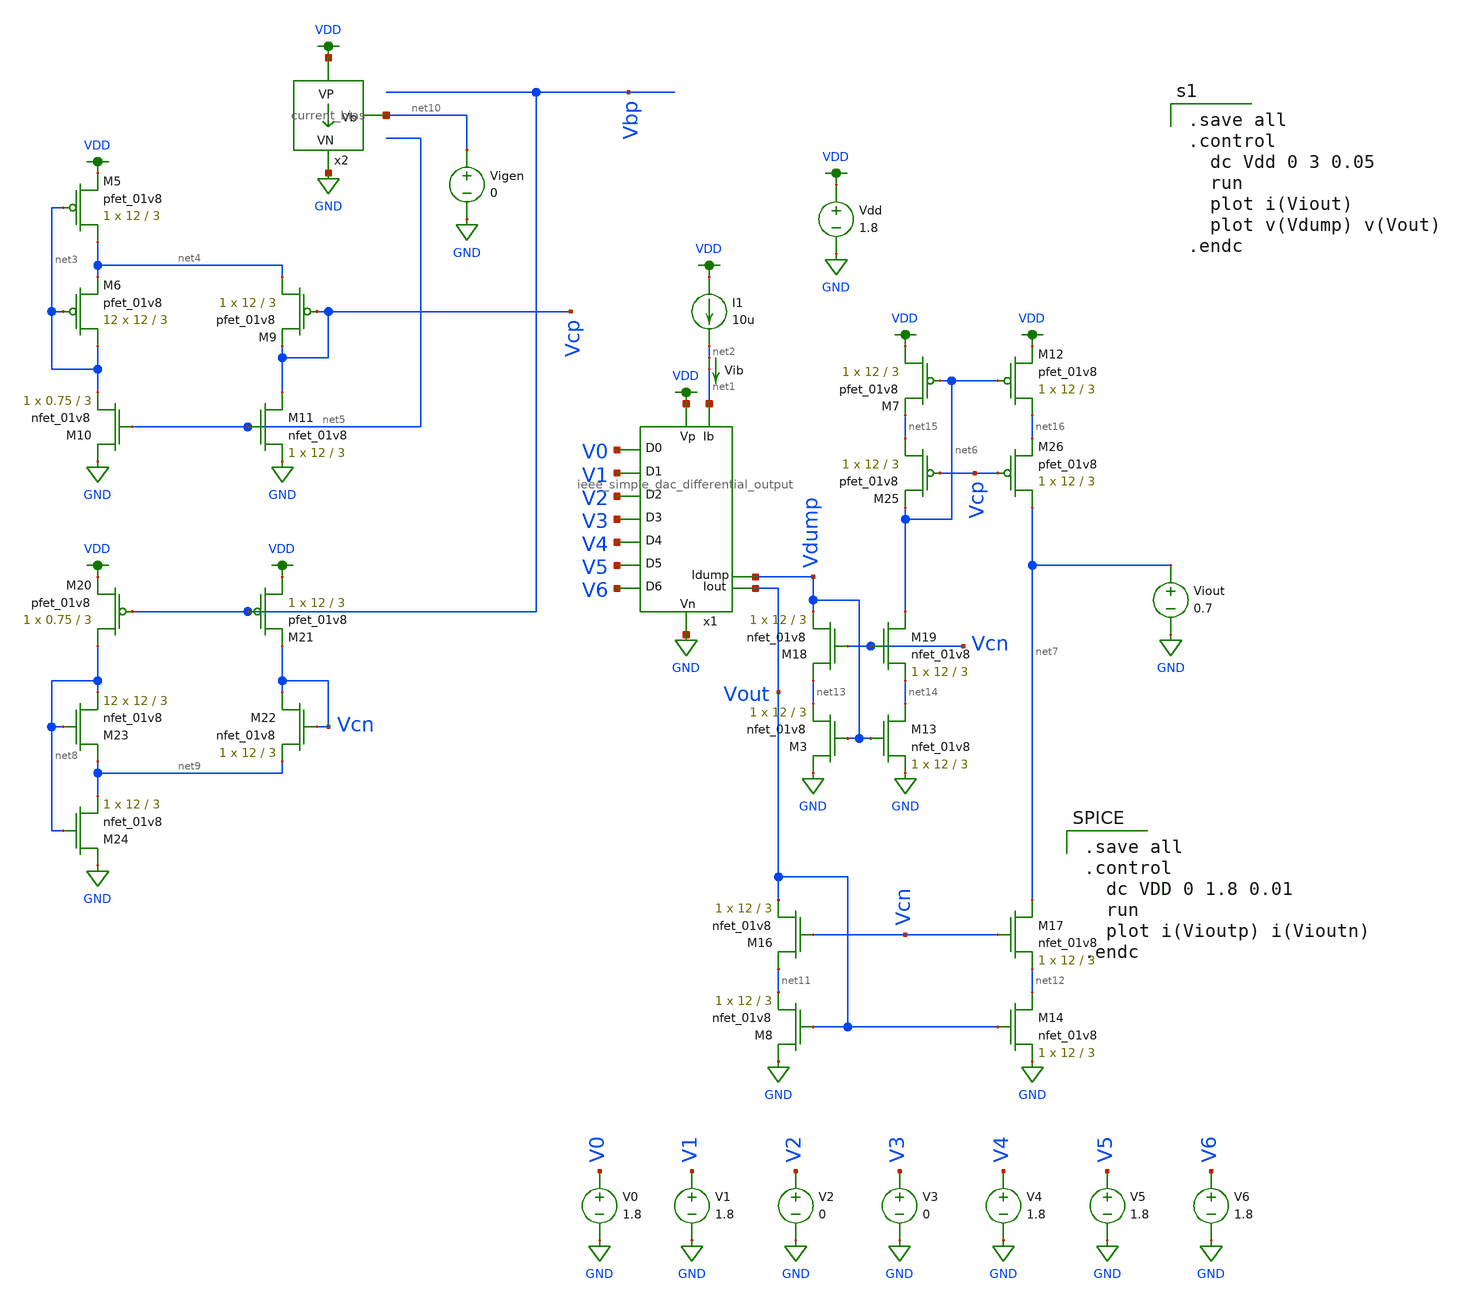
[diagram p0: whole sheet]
** sch_path: schematics/ieee DAC/ieee_DAC_mc_simulation_4.sch
**.subckt ieee_DAC_mc_simulation_4
Vdd VDD GND 1.8
V1 V1 GND 1.8
V2 V2 GND 0
V3 V3 GND 0
V4 V4 GND 1.8
V5 V5 GND 1.8
V6 V6 GND 1.8
V0 V0 GND 1.8
Vib net2 net1 0
.save i(vib)
XM5 net4 net3 VDD VDD sky130_fd_pr__pfet_01v8 L=3 W=12 nf=1 ad='int((nf+1)/2) * W/nf * 0.29' as='int((nf+2)/2) * W/nf * 0.29'
+ pd='2*int((nf+1)/2) * (W/nf + 0.29)' ps='2*int((nf+2)/2) * (W/nf + 0.29)' nrd='0.29 / W' nrs='0.29 / W'
+ sa=0 sb=0 sd=0 mult=1 m=1
XM6 net3 net3 net4 VDD sky130_fd_pr__pfet_01v8 L=3 W=12 nf=1 ad='int((nf+1)/2) * W/nf * 0.29' as='int((nf+2)/2) * W/nf * 0.29'
+ pd='2*int((nf+1)/2) * (W/nf + 0.29)' ps='2*int((nf+2)/2) * (W/nf + 0.29)' nrd='0.29 / W' nrs='0.29 / W'
+ sa=0 sb=0 sd=0 mult=12 m=12
XM9 net4 Vcp Vcp VDD sky130_fd_pr__pfet_01v8 L=3 W=12 nf=1 ad='int((nf+1)/2) * W/nf * 0.29' as='int((nf+2)/2) * W/nf * 0.29'
+ pd='2*int((nf+1)/2) * (W/nf + 0.29)' ps='2*int((nf+2)/2) * (W/nf + 0.29)' nrd='0.29 / W' nrs='0.29 / W'
+ sa=0 sb=0 sd=0 mult=1 m=1
XM10 GND net5 net3 GND sky130_fd_pr__nfet_01v8 L=3 W=0.75 nf=1 ad='int((nf+1)/2) * W/nf * 0.29' as='int((nf+2)/2) * W/nf * 0.29'
+ pd='2*int((nf+1)/2) * (W/nf + 0.29)' ps='2*int((nf+2)/2) * (W/nf + 0.29)' nrd='0.29 / W' nrs='0.29 / W'
+ sa=0 sb=0 sd=0 mult=1 m=1
XM11 Vcp net5 GND GND sky130_fd_pr__nfet_01v8 L=3 W=12 nf=1 ad='int((nf+1)/2) * W/nf * 0.29' as='int((nf+2)/2) * W/nf * 0.29'
+ pd='2*int((nf+1)/2) * (W/nf + 0.29)' ps='2*int((nf+2)/2) * (W/nf + 0.29)' nrd='0.29 / W' nrs='0.29 / W'
+ sa=0 sb=0 sd=0 mult=1 m=1
x2 VDD net10 GND current_bias
Vigen net10 GND 0
x1 VDD Vdump GND V1 V0 V2 V3 V4 V5 V6 net1 Vout ieee_simple_dac_differential_output
XM3 GND Vdump net13 GND sky130_fd_pr__nfet_01v8 L=3 W=12 nf=1 ad='int((nf+1)/2) * W/nf * 0.29' as='int((nf+2)/2) * W/nf * 0.29'
+ pd='2*int((nf+1)/2) * (W/nf + 0.29)' ps='2*int((nf+2)/2) * (W/nf + 0.29)' nrd='0.29 / W' nrs='0.29 / W'
+ sa=0 sb=0 sd=0 mult=1 m=1
XM7 VDD net6 net15 VDD sky130_fd_pr__pfet_01v8 L=3 W=12 nf=1 ad='int((nf+1)/2) * W/nf * 0.29' as='int((nf+2)/2) * W/nf * 0.29'
+ pd='2*int((nf+1)/2) * (W/nf + 0.29)' ps='2*int((nf+2)/2) * (W/nf + 0.29)' nrd='0.29 / W' nrs='0.29 / W'
+ sa=0 sb=0 sd=0 mult=1 m=1
XM8 GND Vout net11 GND sky130_fd_pr__nfet_01v8 L=3 W=12 nf=1 ad='int((nf+1)/2) * W/nf * 0.29' as='int((nf+2)/2) * W/nf * 0.29'
+ pd='2*int((nf+1)/2) * (W/nf + 0.29)' ps='2*int((nf+2)/2) * (W/nf + 0.29)' nrd='0.29 / W' nrs='0.29 / W'
+ sa=0 sb=0 sd=0 mult=1 m=1
XM12 net16 net6 VDD VDD sky130_fd_pr__pfet_01v8 L=3 W=12 nf=1 ad='int((nf+1)/2) * W/nf * 0.29' as='int((nf+2)/2) * W/nf * 0.29'
+ pd='2*int((nf+1)/2) * (W/nf + 0.29)' ps='2*int((nf+2)/2) * (W/nf + 0.29)' nrd='0.29 / W' nrs='0.29 / W'
+ sa=0 sb=0 sd=0 mult=1 m=1
Viout net7 GND 0.7
XM13 net14 Vdump GND GND sky130_fd_pr__nfet_01v8 L=3 W=12 nf=1 ad='int((nf+1)/2) * W/nf * 0.29' as='int((nf+2)/2) * W/nf * 0.29'
+ pd='2*int((nf+1)/2) * (W/nf + 0.29)' ps='2*int((nf+2)/2) * (W/nf + 0.29)' nrd='0.29 / W' nrs='0.29 / W'
+ sa=0 sb=0 sd=0 mult=1 m=1
XM14 net12 Vout GND GND sky130_fd_pr__nfet_01v8 L=3 W=12 nf=1 ad='int((nf+1)/2) * W/nf * 0.29' as='int((nf+2)/2) * W/nf * 0.29'
+ pd='2*int((nf+1)/2) * (W/nf + 0.29)' ps='2*int((nf+2)/2) * (W/nf + 0.29)' nrd='0.29 / W' nrs='0.29 / W'
+ sa=0 sb=0 sd=0 mult=1 m=1
XM20 net8 Vbp VDD VDD sky130_fd_pr__pfet_01v8 L=3 W=0.75 nf=1 ad='int((nf+1)/2) * W/nf * 0.29' as='int((nf+2)/2) * W/nf * 0.29'
+ pd='2*int((nf+1)/2) * (W/nf + 0.29)' ps='2*int((nf+2)/2) * (W/nf + 0.29)' nrd='0.29 / W' nrs='0.29 / W'
+ sa=0 sb=0 sd=0 mult=1 m=1
XM21 VDD Vbp Vcn VDD sky130_fd_pr__pfet_01v8 L=3 W=12 nf=1 ad='int((nf+1)/2) * W/nf * 0.29' as='int((nf+2)/2) * W/nf * 0.29'
+ pd='2*int((nf+1)/2) * (W/nf + 0.29)' ps='2*int((nf+2)/2) * (W/nf + 0.29)' nrd='0.29 / W' nrs='0.29 / W'
+ sa=0 sb=0 sd=0 mult=1 m=1
XM22 Vcn Vcn net9 GND sky130_fd_pr__nfet_01v8 L=3 W=12 nf=1 ad='int((nf+1)/2) * W/nf * 0.29' as='int((nf+2)/2) * W/nf * 0.29'
+ pd='2*int((nf+1)/2) * (W/nf + 0.29)' ps='2*int((nf+2)/2) * (W/nf + 0.29)' nrd='0.29 / W' nrs='0.29 / W'
+ sa=0 sb=0 sd=0 mult=1 m=1
XM23 net9 net8 net8 GND sky130_fd_pr__nfet_01v8 L=3 W=12 nf=1 ad='int((nf+1)/2) * W/nf * 0.29' as='int((nf+2)/2) * W/nf * 0.29'
+ pd='2*int((nf+1)/2) * (W/nf + 0.29)' ps='2*int((nf+2)/2) * (W/nf + 0.29)' nrd='0.29 / W' nrs='0.29 / W'
+ sa=0 sb=0 sd=0 mult=12 m=12
XM24 GND net8 net9 GND sky130_fd_pr__nfet_01v8 L=3 W=12 nf=1 ad='int((nf+1)/2) * W/nf * 0.29' as='int((nf+2)/2) * W/nf * 0.29'
+ pd='2*int((nf+1)/2) * (W/nf + 0.29)' ps='2*int((nf+2)/2) * (W/nf + 0.29)' nrd='0.29 / W' nrs='0.29 / W'
+ sa=0 sb=0 sd=0 mult=1 m=1
XM16 net11 Vcn Vout GND sky130_fd_pr__nfet_01v8 L=3 W=12 nf=1 ad='int((nf+1)/2) * W/nf * 0.29' as='int((nf+2)/2) * W/nf * 0.29'
+ pd='2*int((nf+1)/2) * (W/nf + 0.29)' ps='2*int((nf+2)/2) * (W/nf + 0.29)' nrd='0.29 / W' nrs='0.29 / W'
+ sa=0 sb=0 sd=0 mult=1 m=1
XM17 net7 Vcn net12 GND sky130_fd_pr__nfet_01v8 L=3 W=12 nf=1 ad='int((nf+1)/2) * W/nf * 0.29' as='int((nf+2)/2) * W/nf * 0.29'
+ pd='2*int((nf+1)/2) * (W/nf + 0.29)' ps='2*int((nf+2)/2) * (W/nf + 0.29)' nrd='0.29 / W' nrs='0.29 / W'
+ sa=0 sb=0 sd=0 mult=1 m=1
XM18 net13 Vcn Vdump GND sky130_fd_pr__nfet_01v8 L=3 W=12 nf=1 ad='int((nf+1)/2) * W/nf * 0.29' as='int((nf+2)/2) * W/nf * 0.29'
+ pd='2*int((nf+1)/2) * (W/nf + 0.29)' ps='2*int((nf+2)/2) * (W/nf + 0.29)' nrd='0.29 / W' nrs='0.29 / W'
+ sa=0 sb=0 sd=0 mult=1 m=1
XM19 net6 Vcn net14 GND sky130_fd_pr__nfet_01v8 L=3 W=12 nf=1 ad='int((nf+1)/2) * W/nf * 0.29' as='int((nf+2)/2) * W/nf * 0.29'
+ pd='2*int((nf+1)/2) * (W/nf + 0.29)' ps='2*int((nf+2)/2) * (W/nf + 0.29)' nrd='0.29 / W' nrs='0.29 / W'
+ sa=0 sb=0 sd=0 mult=1 m=1
XM25 net15 Vcp net6 VDD sky130_fd_pr__pfet_01v8 L=3 W=12 nf=1 ad='int((nf+1)/2) * W/nf * 0.29' as='int((nf+2)/2) * W/nf * 0.29'
+ pd='2*int((nf+1)/2) * (W/nf + 0.29)' ps='2*int((nf+2)/2) * (W/nf + 0.29)' nrd='0.29 / W' nrs='0.29 / W'
+ sa=0 sb=0 sd=0 mult=1 m=1
XM26 net7 Vcp net16 VDD sky130_fd_pr__pfet_01v8 L=3 W=12 nf=1 ad='int((nf+1)/2) * W/nf * 0.29' as='int((nf+2)/2) * W/nf * 0.29'
+ pd='2*int((nf+1)/2) * (W/nf + 0.29)' ps='2*int((nf+2)/2) * (W/nf + 0.29)' nrd='0.29 / W' nrs='0.29 / W'
+ sa=0 sb=0 sd=0 mult=1 m=1
I1 VDD net2 10u
**** begin user architecture code

.option wnflag=1
.param MC_SWITCH=1.0
.lib ~/skywater/skywater-pdk/libraries/sky130_fd_pr_ngspice/latest/models/sky130.lib.spice tt


.save all
.control
  dc Vdd 0 3 0.05
  run
  plot i(Viout)
  plot v(Vdump) v(Vout)
.endc


.save all
.control
  dc VDD 0 1.8 0.01
  run
  plot i(Vioutp) i(Vioutn)
.endc

**** end user architecture code
**.ends
.GLOBAL VDD
.GLOBAL GND
.end
